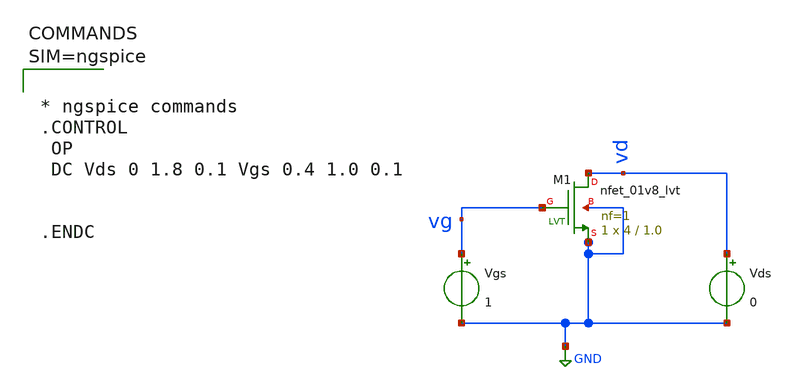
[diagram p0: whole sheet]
** sch_path: work/xschem/trans_nmos1.sch
**.subckt trans_nmos1
XM1 vd vg GND GND sky130_fd_pr__nfet_01v8_lvt L=1.0 W=4 nf=1 ad='int((1 + 1)/2) * 4 / 1 * 0.29' as='int((1 + 2)/2) * 4 / 1 * 0.29'
+ pd='2*int((1 + 1)/2) * (4 / 1 + 0.29)' ps='2*int((1 + 2)/2) * (4 / 1 + 0.29)' nrd='0.29 / 4 ' nrs='0.29 / 4 '
+ sa=0 sb=0 sd=0 mult=1 m=1
Vgs vg GND 1
Vds vd GND 0
**** begin user architecture code



* ngspice commands
.CONTROL
 OP
 DC Vds 0 1.8 0.1 Vgs 0.4 1.0 0.1


.ENDC




** opencircuitdesign pdks install
.lib $::SKYWATER_MODELS/sky130.lib.spice tt


** opencircuitdesign pdks install
.lib $::SKYWATER_MODELS/sky130.lib.spice tt

**** end user architecture code
**.ends
.GLOBAL GND
.end
